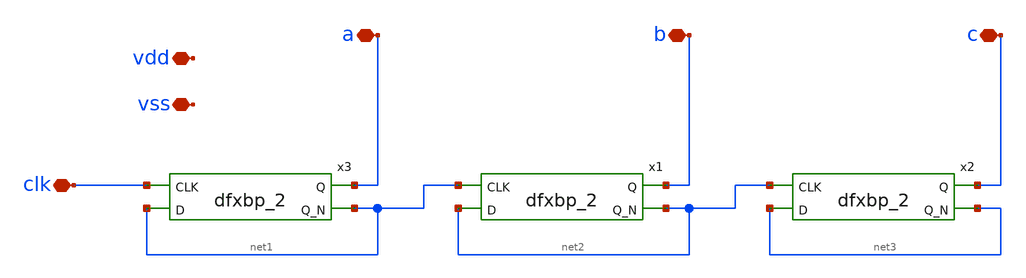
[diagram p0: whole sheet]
** sch_path: xschem01/divider/untitled-3.sch
**.subckt untitled-3 clk vdd vss a b c
*.iopin clk
*.iopin vdd
*.iopin vss
*.iopin a
*.iopin b
*.iopin c
x3 clk net1 VSS VSS VDD VDD a net1 sky130_fd_sc_hd__dfxbp_2
x1 net1 net2 VSS VSS VDD VDD b net2 sky130_fd_sc_hd__dfxbp_2
x2 net2 net3 VSS VSS VDD VDD c net3 sky130_fd_sc_hd__dfxbp_2
**.ends
.end
